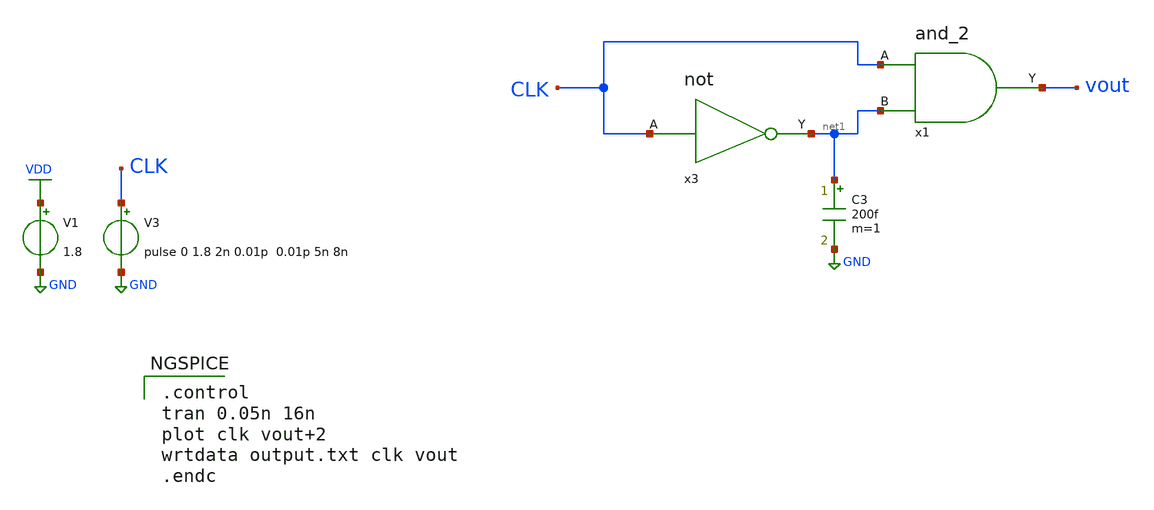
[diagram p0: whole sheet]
** sch_path: Circuiti/pulse.sch
**.subckt pulse
V1 VDD GND 1.8
x3 CLK net1 not
C3 net1 GND 200f m=1
x1 CLK vout net1 and_2
V3 CLK GND pulse 0 1.8 2n 0.01p 0.01p 5n 8n
**** begin user architecture code


.lib /home/matteo/xschem_downloads/skywater-pdk/libraries/sky130_fd_pr_ngspice/latest/models/sky130.lib.spice tt

*.include /home/matteo/xschem_downloads/skywater-pdk/libraries/sky130_fd_pr_ngspice/latest/cells/nfet_01v8/sky130_fd_pr__nfet_01v8__tt.corner.spice

.param mc_mm_switch=0
.param mc_pr_switch=1



.control
tran 0.05n 16n
plot clk vout+2
wrtdata output.txt clk vout
.endc


**** end user architecture code
**.ends

* expanding   symbol:  /home/matteo/Documenti/tesi/Circuiti/logic_gates_sch_sym/not.sym # of pins=2
** sym_path: Circuiti/logic_gates_sch_sym/not.sym
** sch_path: Circuiti/logic_gates_sch_sym/not.sch
.subckt not A Y
*.ipin A
*.opin Y
XM1 Y A GND GND sky130_fd_pr__nfet_01v8 L=0.45 W=1 nf=1 ad='int((nf+1)/2) * W/nf * 0.29' as='int((nf+2)/2) * W/nf * 0.29'
+ pd='2*int((nf+1)/2) * (W/nf + 0.29)' ps='2*int((nf+2)/2) * (W/nf + 0.29)' nrd='0.29 / W' nrs='0.29 / W'
+ sa=0 sb=0 sd=0 mult=1 m=1
XM2 Y A Vdd VDD sky130_fd_pr__pfet_01v8 L=0.45 W=4.8 nf=1 ad='int((nf+1)/2) * W/nf * 0.29' as='int((nf+2)/2) * W/nf * 0.29'
+ pd='2*int((nf+1)/2) * (W/nf + 0.29)' ps='2*int((nf+2)/2) * (W/nf + 0.29)' nrd='0.29 / W' nrs='0.29 / W'
+ sa=0 sb=0 sd=0 mult=1 m=1
.ends


* expanding   symbol:  /home/matteo/Documenti/tesi/Circuiti/logic_gates_sch_sym/and_2.sym # of
*+ pins=3
** sym_path: Circuiti/logic_gates_sch_sym/and_2.sym
** sch_path: Circuiti/logic_gates_sch_sym/and_2.sch
.subckt and_2 A Y B
*.ipin B
*.ipin A
*.opin Y
x1 A net1 B nand_2
x2 net1 Y not
.ends


* expanding   symbol:  /home/matteo/Documenti/tesi/Circuiti/logic_gates_sch_sym/nand_2.sym # of
*+ pins=3
** sym_path: Circuiti/logic_gates_sch_sym/nand_2.sym
** sch_path: Circuiti/logic_gates_sch_sym/nand_2.sch
.subckt nand_2 A Y B
*.ipin A
*.ipin B
*.opin Y
XM1 Y A net1 GND sky130_fd_pr__nfet_01v8 L=0.15 W=1 nf=1 ad='int((nf+1)/2) * W/nf * 0.29' as='int((nf+2)/2) * W/nf * 0.29'
+ pd='2*int((nf+1)/2) * (W/nf + 0.29)' ps='2*int((nf+2)/2) * (W/nf + 0.29)' nrd='0.29 / W' nrs='0.29 / W'
+ sa=0 sb=0 sd=0 mult=1 m=1
XM3 Y B Vdd VDD sky130_fd_pr__pfet_01v8 L=0.45 W=4.8 nf=1 ad='int((nf+1)/2) * W/nf * 0.29' as='int((nf+2)/2) * W/nf * 0.29'
+ pd='2*int((nf+1)/2) * (W/nf + 0.29)' ps='2*int((nf+2)/2) * (W/nf + 0.29)' nrd='0.29 / W' nrs='0.29 / W'
+ sa=0 sb=0 sd=0 mult=1 m=1
XM4 Y A Vdd VDD sky130_fd_pr__pfet_01v8 L=0.45 W=4.8 nf=1 ad='int((nf+1)/2) * W/nf * 0.29' as='int((nf+2)/2) * W/nf * 0.29'
+ pd='2*int((nf+1)/2) * (W/nf + 0.29)' ps='2*int((nf+2)/2) * (W/nf + 0.29)' nrd='0.29 / W' nrs='0.29 / W'
+ sa=0 sb=0 sd=0 mult=1 m=1
XM2 net1 B GND GND sky130_fd_pr__nfet_01v8 L=0.15 W=1 nf=1 ad='int((nf+1)/2) * W/nf * 0.29' as='int((nf+2)/2) * W/nf * 0.29'
+ pd='2*int((nf+1)/2) * (W/nf + 0.29)' ps='2*int((nf+2)/2) * (W/nf + 0.29)' nrd='0.29 / W' nrs='0.29 / W'
+ sa=0 sb=0 sd=0 mult=1 m=1
.ends

.GLOBAL GND
.GLOBAL VDD
.GLOBAL Vdd
.end
